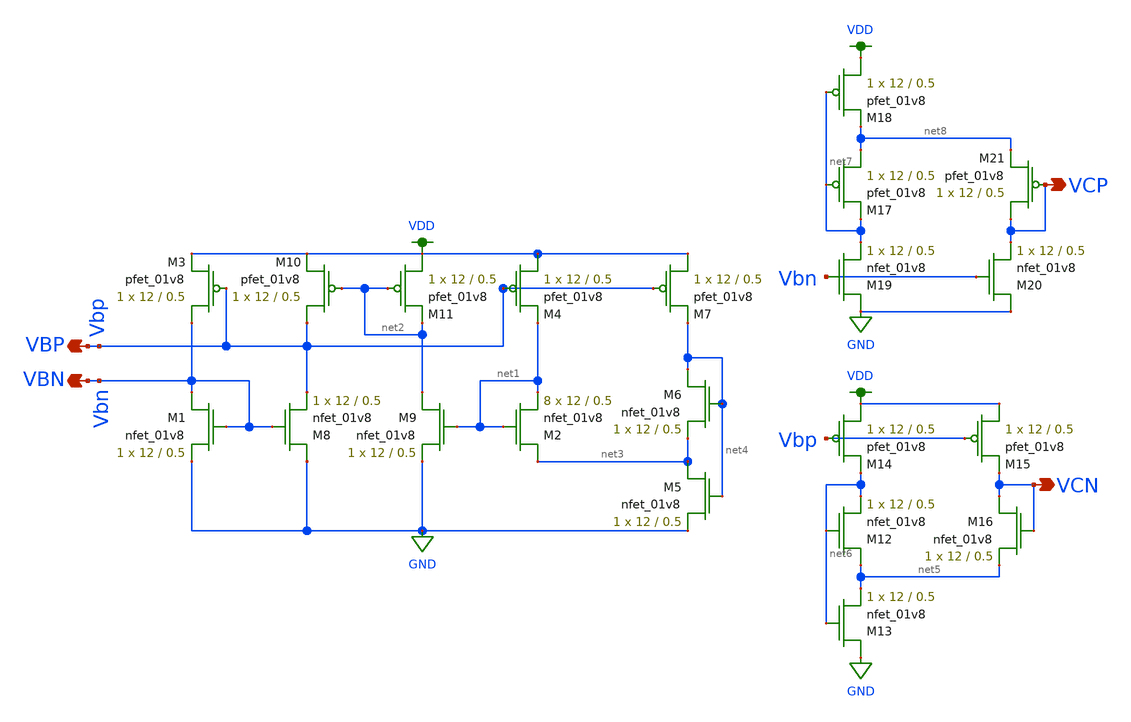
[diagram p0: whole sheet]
** sch_path: miniproject_03/xschem/bias_gen.sch
**.subckt bias_gen VBP VBN VCP VCN
*.opin VBP
*.opin VBN
*.opin VCP
*.opin VCN
XM2 net3 net1 net1 GND sky130_fd_pr__nfet_01v8 L=0.5 W=12 nf=1 ad='int((nf+1)/2) * W/nf * 0.29' as='int((nf+2)/2) * W/nf * 0.29'
+ pd='2*int((nf+1)/2) * (W/nf + 0.29)' ps='2*int((nf+2)/2) * (W/nf + 0.29)' nrd='0.29 / W' nrs='0.29 / W'
+ sa=0 sb=0 sd=0 mult=8 m=8
XM11 VDD net2 net2 VDD sky130_fd_pr__pfet_01v8 L=0.5 W=12 nf=1 ad='int((nf+1)/2) * W/nf * 0.29' as='int((nf+2)/2) * W/nf * 0.29'
+ pd='2*int((nf+1)/2) * (W/nf + 0.29)' ps='2*int((nf+2)/2) * (W/nf + 0.29)' nrd='0.29 / W' nrs='0.29 / W'
+ sa=0 sb=0 sd=0 mult=1 m=1
XM1 Vbn Vbn GND GND sky130_fd_pr__nfet_01v8 L=0.5 W=12 nf=1 ad='int((nf+1)/2) * W/nf * 0.29' as='int((nf+2)/2) * W/nf * 0.29'
+ pd='2*int((nf+1)/2) * (W/nf + 0.29)' ps='2*int((nf+2)/2) * (W/nf + 0.29)' nrd='0.29 / W' nrs='0.29 / W'
+ sa=0 sb=0 sd=0 mult=1 m=1
XM4 VDD Vbp net1 VDD sky130_fd_pr__pfet_01v8 L=0.5 W=12 nf=1 ad='int((nf+1)/2) * W/nf * 0.29' as='int((nf+2)/2) * W/nf * 0.29'
+ pd='2*int((nf+1)/2) * (W/nf + 0.29)' ps='2*int((nf+2)/2) * (W/nf + 0.29)' nrd='0.29 / W' nrs='0.29 / W'
+ sa=0 sb=0 sd=0 mult=1 m=1
XM10 Vbp net2 VDD VDD sky130_fd_pr__pfet_01v8 L=0.5 W=12 nf=1 ad='int((nf+1)/2) * W/nf * 0.29' as='int((nf+2)/2) * W/nf * 0.29'
+ pd='2*int((nf+1)/2) * (W/nf + 0.29)' ps='2*int((nf+2)/2) * (W/nf + 0.29)' nrd='0.29 / W' nrs='0.29 / W'
+ sa=0 sb=0 sd=0 mult=1 m=1
XM3 Vbn Vbp VDD VDD sky130_fd_pr__pfet_01v8 L=0.5 W=12 nf=1 ad='int((nf+1)/2) * W/nf * 0.29' as='int((nf+2)/2) * W/nf * 0.29'
+ pd='2*int((nf+1)/2) * (W/nf + 0.29)' ps='2*int((nf+2)/2) * (W/nf + 0.29)' nrd='0.29 / W' nrs='0.29 / W'
+ sa=0 sb=0 sd=0 mult=1 m=1
XM8 GND Vbn Vbp GND sky130_fd_pr__nfet_01v8 L=0.5 W=12 nf=1 ad='int((nf+1)/2) * W/nf * 0.29' as='int((nf+2)/2) * W/nf * 0.29'
+ pd='2*int((nf+1)/2) * (W/nf + 0.29)' ps='2*int((nf+2)/2) * (W/nf + 0.29)' nrd='0.29 / W' nrs='0.29 / W'
+ sa=0 sb=0 sd=0 mult=1 m=1
XM9 net2 net1 GND GND sky130_fd_pr__nfet_01v8 L=0.5 W=12 nf=1 ad='int((nf+1)/2) * W/nf * 0.29' as='int((nf+2)/2) * W/nf * 0.29'
+ pd='2*int((nf+1)/2) * (W/nf + 0.29)' ps='2*int((nf+2)/2) * (W/nf + 0.29)' nrd='0.29 / W' nrs='0.29 / W'
+ sa=0 sb=0 sd=0 mult=1 m=1
XM6 net4 net4 net3 GND sky130_fd_pr__nfet_01v8 L=0.5 W=12 nf=1 ad='int((nf+1)/2) * W/nf * 0.29' as='int((nf+2)/2) * W/nf * 0.29'
+ pd='2*int((nf+1)/2) * (W/nf + 0.29)' ps='2*int((nf+2)/2) * (W/nf + 0.29)' nrd='0.29 / W' nrs='0.29 / W'
+ sa=0 sb=0 sd=0 mult=1 m=1
XM5 net3 net4 GND GND sky130_fd_pr__nfet_01v8 L=0.5 W=12 nf=1 ad='int((nf+1)/2) * W/nf * 0.29' as='int((nf+2)/2) * W/nf * 0.29'
+ pd='2*int((nf+1)/2) * (W/nf + 0.29)' ps='2*int((nf+2)/2) * (W/nf + 0.29)' nrd='0.29 / W' nrs='0.29 / W'
+ sa=0 sb=0 sd=0 mult=1 m=1
XM7 VDD Vbp net4 VDD sky130_fd_pr__pfet_01v8 L=0.5 W=12 nf=1 ad='int((nf+1)/2) * W/nf * 0.29' as='int((nf+2)/2) * W/nf * 0.29'
+ pd='2*int((nf+1)/2) * (W/nf + 0.29)' ps='2*int((nf+2)/2) * (W/nf + 0.29)' nrd='0.29 / W' nrs='0.29 / W'
+ sa=0 sb=0 sd=0 mult=1 m=1
XM12 net5 net6 net6 GND sky130_fd_pr__nfet_01v8 L=0.5 W=12 nf=1 ad='int((nf+1)/2) * W/nf * 0.29' as='int((nf+2)/2) * W/nf * 0.29'
+ pd='2*int((nf+1)/2) * (W/nf + 0.29)' ps='2*int((nf+2)/2) * (W/nf + 0.29)' nrd='0.29 / W' nrs='0.29 / W'
+ sa=0 sb=0 sd=0 mult=1 m=1
XM14 VDD Vbp net6 VDD sky130_fd_pr__pfet_01v8 L=0.5 W=12 nf=1 ad='int((nf+1)/2) * W/nf * 0.29' as='int((nf+2)/2) * W/nf * 0.29'
+ pd='2*int((nf+1)/2) * (W/nf + 0.29)' ps='2*int((nf+2)/2) * (W/nf + 0.29)' nrd='0.29 / W' nrs='0.29 / W'
+ sa=0 sb=0 sd=0 mult=1 m=1
XM13 GND net6 net5 GND sky130_fd_pr__nfet_01v8 L=0.5 W=12 nf=1 ad='int((nf+1)/2) * W/nf * 0.29' as='int((nf+2)/2) * W/nf * 0.29'
+ pd='2*int((nf+1)/2) * (W/nf + 0.29)' ps='2*int((nf+2)/2) * (W/nf + 0.29)' nrd='0.29 / W' nrs='0.29 / W'
+ sa=0 sb=0 sd=0 mult=1 m=1
XM15 VDD Vbp VCN VDD sky130_fd_pr__pfet_01v8 L=0.5 W=12 nf=1 ad='int((nf+1)/2) * W/nf * 0.29' as='int((nf+2)/2) * W/nf * 0.29'
+ pd='2*int((nf+1)/2) * (W/nf + 0.29)' ps='2*int((nf+2)/2) * (W/nf + 0.29)' nrd='0.29 / W' nrs='0.29 / W'
+ sa=0 sb=0 sd=0 mult=1 m=1
XM16 VCN VCN net5 GND sky130_fd_pr__nfet_01v8 L=0.5 W=12 nf=1 ad='int((nf+1)/2) * W/nf * 0.29' as='int((nf+2)/2) * W/nf * 0.29'
+ pd='2*int((nf+1)/2) * (W/nf + 0.29)' ps='2*int((nf+2)/2) * (W/nf + 0.29)' nrd='0.29 / W' nrs='0.29 / W'
+ sa=0 sb=0 sd=0 mult=1 m=1
XM17 net8 net7 net7 VDD sky130_fd_pr__pfet_01v8 L=0.5 W=12 nf=1 ad='int((nf+1)/2) * W/nf * 0.29' as='int((nf+2)/2) * W/nf * 0.29'
+ pd='2*int((nf+1)/2) * (W/nf + 0.29)' ps='2*int((nf+2)/2) * (W/nf + 0.29)' nrd='0.29 / W' nrs='0.29 / W'
+ sa=0 sb=0 sd=0 mult=1 m=1
XM18 VDD net7 net8 VDD sky130_fd_pr__pfet_01v8 L=0.5 W=12 nf=1 ad='int((nf+1)/2) * W/nf * 0.29' as='int((nf+2)/2) * W/nf * 0.29'
+ pd='2*int((nf+1)/2) * (W/nf + 0.29)' ps='2*int((nf+2)/2) * (W/nf + 0.29)' nrd='0.29 / W' nrs='0.29 / W'
+ sa=0 sb=0 sd=0 mult=1 m=1
XM19 GND Vbn net7 GND sky130_fd_pr__nfet_01v8 L=0.5 W=12 nf=1 ad='int((nf+1)/2) * W/nf * 0.29' as='int((nf+2)/2) * W/nf * 0.29'
+ pd='2*int((nf+1)/2) * (W/nf + 0.29)' ps='2*int((nf+2)/2) * (W/nf + 0.29)' nrd='0.29 / W' nrs='0.29 / W'
+ sa=0 sb=0 sd=0 mult=1 m=1
XM20 GND Vbn VCP GND sky130_fd_pr__nfet_01v8 L=0.5 W=12 nf=1 ad='int((nf+1)/2) * W/nf * 0.29' as='int((nf+2)/2) * W/nf * 0.29'
+ pd='2*int((nf+1)/2) * (W/nf + 0.29)' ps='2*int((nf+2)/2) * (W/nf + 0.29)' nrd='0.29 / W' nrs='0.29 / W'
+ sa=0 sb=0 sd=0 mult=1 m=1
XM21 VCP VCP net8 VDD sky130_fd_pr__pfet_01v8 L=0.5 W=12 nf=1 ad='int((nf+1)/2) * W/nf * 0.29' as='int((nf+2)/2) * W/nf * 0.29'
+ pd='2*int((nf+1)/2) * (W/nf + 0.29)' ps='2*int((nf+2)/2) * (W/nf + 0.29)' nrd='0.29 / W' nrs='0.29 / W'
+ sa=0 sb=0 sd=0 mult=1 m=1
**.ends
.GLOBAL VDD
.GLOBAL GND
.end
